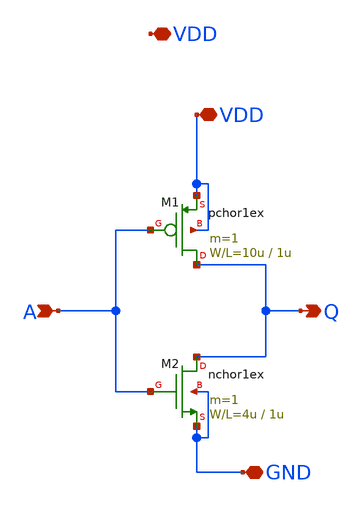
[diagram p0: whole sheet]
** sch_path: member_project/1uf3/inverter.sch
**.subckt inverter Q A VDD VDD GND
*.opin Q
*.ipin A
*.iopin VDD
*.iopin VDD
*.iopin GND
M1 Q A VDD VDD pchor1ex L=1u W=10u m=1
M2 Q A GND GND nchor1ex L=1u W=4u m=1
**.ends
.end
